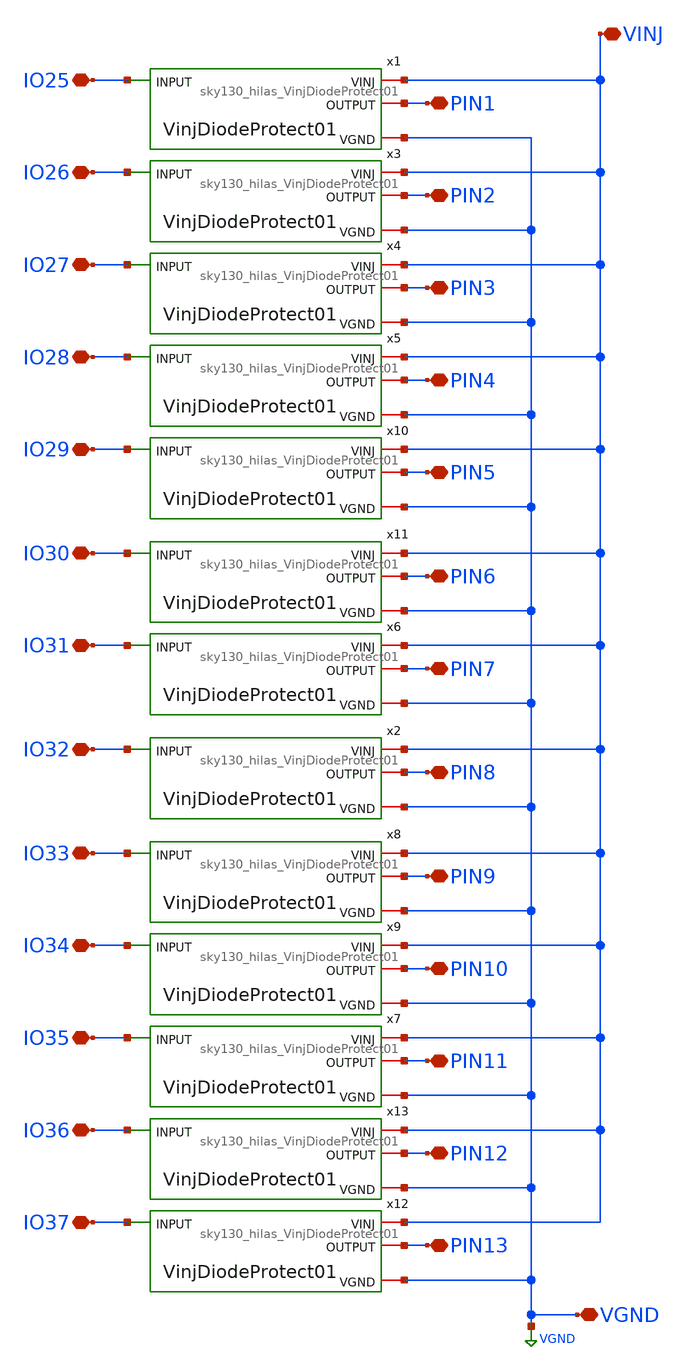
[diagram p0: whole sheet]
** sch_path: libs.ref/sky130_hilas_sc/xschem/sky130_hilas_LeftProtection.sch
**.subckt sky130_hilas_LeftProtection PIN1 IO25 IO26 PIN11 IO27 IO28 IO29 IO30 IO31 IO33 IO34 IO35
*+ PIN2 PIN3 PIN4 PIN5 PIN6 PIN7 PIN8 PIN9 PIN10 VINJ IO36 IO37 PIN12 PIN13 IO32 VGND
*.iopin PIN1
*.iopin IO25
*.iopin IO26
*.iopin PIN11
*.iopin IO27
*.iopin IO28
*.iopin IO29
*.iopin IO30
*.iopin IO31
*.iopin IO33
*.iopin IO34
*.iopin IO35
*.iopin PIN2
*.iopin PIN3
*.iopin PIN4
*.iopin PIN5
*.iopin PIN6
*.iopin PIN7
*.iopin PIN8
*.iopin PIN9
*.iopin PIN10
*.iopin VINJ
*.iopin IO36
*.iopin IO37
*.iopin PIN12
*.iopin PIN13
*.iopin IO32
*.iopin VGND
x1 VINJ PIN1 IO25 VGND sky130_hilas_VinjDiodeProtect01
x3 VINJ PIN2 IO26 VGND sky130_hilas_VinjDiodeProtect01
x4 VINJ PIN3 IO27 VGND sky130_hilas_VinjDiodeProtect01
x5 VINJ PIN4 IO28 VGND sky130_hilas_VinjDiodeProtect01
x6 VINJ PIN7 IO31 VGND sky130_hilas_VinjDiodeProtect01
x7 VINJ PIN11 IO35 VGND sky130_hilas_VinjDiodeProtect01
x8 VINJ PIN9 IO33 VGND sky130_hilas_VinjDiodeProtect01
x9 VINJ PIN10 IO34 VGND sky130_hilas_VinjDiodeProtect01
x10 VINJ PIN5 IO29 VGND sky130_hilas_VinjDiodeProtect01
x11 VINJ PIN6 IO30 VGND sky130_hilas_VinjDiodeProtect01
x2 VINJ PIN8 IO32 VGND sky130_hilas_VinjDiodeProtect01
x12 VINJ PIN13 IO37 VGND sky130_hilas_VinjDiodeProtect01
x13 VINJ PIN12 IO36 VGND sky130_hilas_VinjDiodeProtect01
**.ends

* expanding   symbol:  sky130_hilas_VinjDiodeProtect01.sym # of pins=4
** sym_path: libs.ref/sky130_hilas_sc/xschem/sky130_hilas_VinjDiodeProtect01.sym
** sch_path: libs.ref/sky130_hilas_sc/xschem/sky130_hilas_VinjDiodeProtect01.sch
.subckt sky130_hilas_VinjDiodeProtect01 VINJ OUTPUT INPUT VGND
*.ipin INPUT
*.iopin VINJ
*.iopin OUTPUT
*.iopin VGND
XD1 OUTPUT VINJ sky130_fd_pr__diode_pw2nd_05v5 area=1 pj=4e6
XD2 VGND OUTPUT sky130_fd_pr__diode_pw2nd_05v5 area=1 pj=4e6
R1 INPUT OUTPUT 100 m=1
.ends

.GLOBAL VGND
.end
